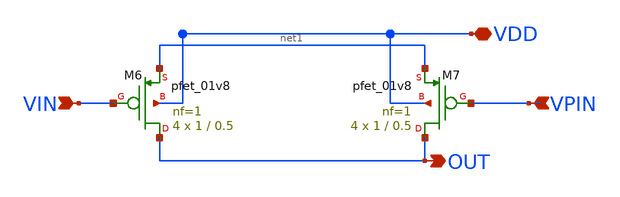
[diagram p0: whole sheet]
** sch_path: untitled.sch
**.subckt untitled VIN OUT VPIN VDD
*.ipin VIN
*.opin OUT
*.ipin VPIN
*.iopin VDD
XM7 OUT VPIN net1 VDD sky130_fd_pr__pfet_01v8 L=0.5 W=1 nf=1 ad='int((nf+1)/2) * W/nf * 0.29' as='int((nf+2)/2) * W/nf * 0.29'
+ pd='2*int((nf+1)/2) * (W/nf + 0.29)' ps='2*int((nf+2)/2) * (W/nf + 0.29)' nrd='0.29 / W' nrs='0.29 / W'
+ sa=0 sb=0 sd=0 mult=4 m=4
XM6 OUT VIN net1 VDD sky130_fd_pr__pfet_01v8 L=0.5 W=1 nf=1 ad='int((nf+1)/2) * W/nf * 0.29' as='int((nf+2)/2) * W/nf * 0.29'
+ pd='2*int((nf+1)/2) * (W/nf + 0.29)' ps='2*int((nf+2)/2) * (W/nf + 0.29)' nrd='0.29 / W' nrs='0.29 / W'
+ sa=0 sb=0 sd=0 mult=4 m=4
**.ends
.end
